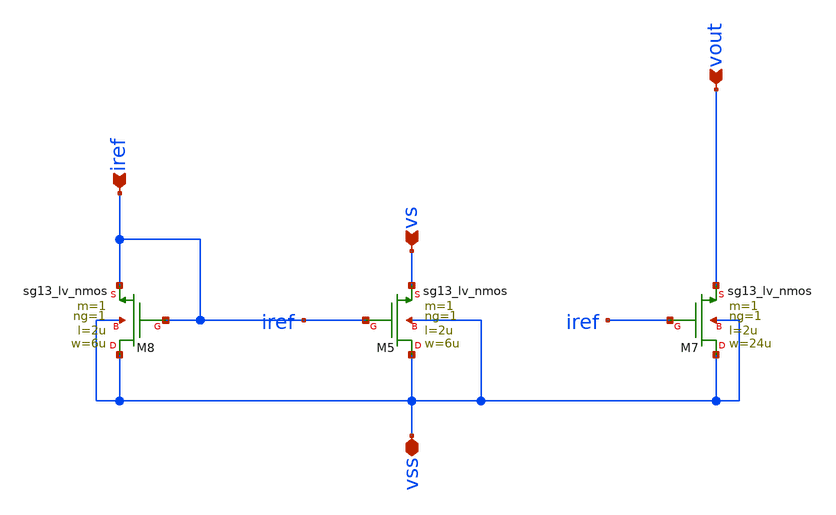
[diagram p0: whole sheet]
** sch_path: AC3E-IHP_ALDO/design_data/klayout/lvs/nmos_cmirror/nmos_current_mirror.sch
**.subckt nmos_current_mirror iref vss vs vout
*.ipin iref
*.iopin vss
*.ipin vs
*.ipin vout
XM5 vss iref vs vss sg13_lv_nmos w=6u l=2u ng=1 m=1 mm_ok=1
XM8 vss iref iref vss sg13_lv_nmos w=6u l=2u ng=1 m=1 mm_ok=1
XM7 vss iref vout vss sg13_lv_nmos w=24u l=2u ng=1 m=1 mm_ok=1
**.ends
.end
